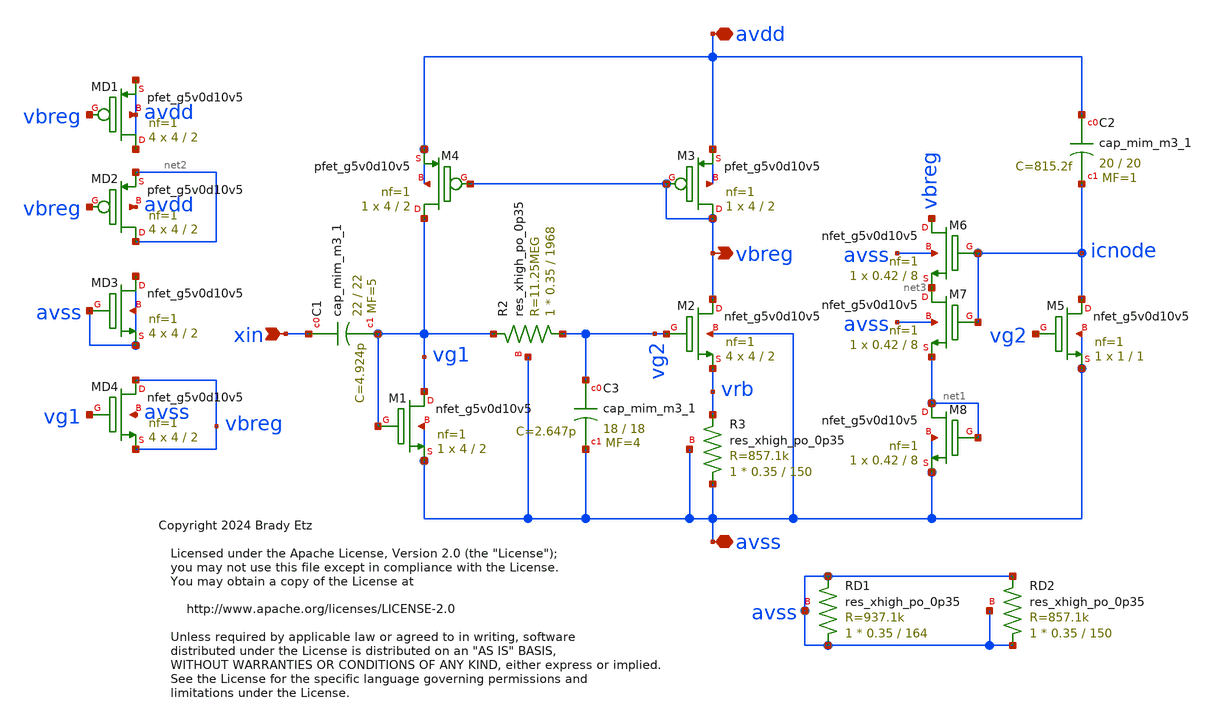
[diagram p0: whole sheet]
** sch_path: xschem/bias_gen.sch
* Copyright 2024 Brady Etz
* Licensed under the Apache License, Version 2.0 (the "License");
**.subckt bias_gen xin avdd avss vbreg
*.ipin xin
*.iopin avdd
*.iopin avss
*.opin vbreg
XM2 vbreg vg2 vrb avss sky130_fd_pr__nfet_g5v0d10v5 L=2 W=4 nf=1 ad='int((nf+1)/2) * W/nf * 0.29' as='int((nf+2)/2) * W/nf * 0.29'
+ pd='2*int((nf+1)/2) * (W/nf + 0.29)' ps='2*int((nf+2)/2) * (W/nf + 0.29)' nrd='0.29 / W' nrs='0.29 / W'
+ sa=0 sb=0 sd=0 mult=4 m=4
XM3 vbreg vbreg avdd avdd sky130_fd_pr__pfet_g5v0d10v5 L=2 W=4 nf=1 ad='int((nf+1)/2) * W/nf * 0.29'
+ as='int((nf+2)/2) * W/nf * 0.29' pd='2*int((nf+1)/2) * (W/nf + 0.29)' ps='2*int((nf+2)/2) * (W/nf + 0.29)'
+ nrd='0.29 / W' nrs='0.29 / W' sa=0 sb=0 sd=0 mult=1 m=1
XM4 vg1 vbreg avdd avdd sky130_fd_pr__pfet_g5v0d10v5 L=2 W=4 nf=1 ad='int((nf+1)/2) * W/nf * 0.29' as='int((nf+2)/2) * W/nf * 0.29'
+ pd='2*int((nf+1)/2) * (W/nf + 0.29)' ps='2*int((nf+2)/2) * (W/nf + 0.29)' nrd='0.29 / W' nrs='0.29 / W'
+ sa=0 sb=0 sd=0 mult=1 m=1
XM1 vg1 vg1 avss avss sky130_fd_pr__nfet_g5v0d10v5 L=2 W=4 nf=1 ad='int((nf+1)/2) * W/nf * 0.29' as='int((nf+2)/2) * W/nf * 0.29'
+ pd='2*int((nf+1)/2) * (W/nf + 0.29)' ps='2*int((nf+2)/2) * (W/nf + 0.29)' nrd='0.29 / W' nrs='0.29 / W'
+ sa=0 sb=0 sd=0 mult=1 m=1
XR2 vg2 vg1 avss sky130_fd_pr__res_xhigh_po_0p35 L=1968 mult=1 m=1
XR3 avss vrb avss sky130_fd_pr__res_xhigh_po_0p35 L=150 mult=1 m=1
XC3 vg2 avss sky130_fd_pr__cap_mim_m3_1 W=18 L=18 MF=4 m=4
XC1 xin vg1 sky130_fd_pr__cap_mim_m3_1 W=22 L=22 MF=5 m=5
XM5 icnode vg2 avss avss sky130_fd_pr__nfet_g5v0d10v5 L=1 W=1 nf=1 ad='int((nf+1)/2) * W/nf * 0.29' as='int((nf+2)/2) * W/nf * 0.29'
+ pd='2*int((nf+1)/2) * (W/nf + 0.29)' ps='2*int((nf+2)/2) * (W/nf + 0.29)' nrd='0.29 / W' nrs='0.29 / W'
+ sa=0 sb=0 sd=0 mult=1 m=1
XC2 avdd icnode sky130_fd_pr__cap_mim_m3_1 W=20 L=20 MF=1 m=1
XM6 vbreg icnode net3 avss sky130_fd_pr__nfet_g5v0d10v5 L=8 W=0.42 nf=1 ad='int((nf+1)/2) * W/nf * 0.29'
+ as='int((nf+2)/2) * W/nf * 0.29' pd='2*int((nf+1)/2) * (W/nf + 0.29)' ps='2*int((nf+2)/2) * (W/nf + 0.29)'
+ nrd='0.29 / W' nrs='0.29 / W' sa=0 sb=0 sd=0 mult=1 m=1
XM8 net1 net1 avss avss sky130_fd_pr__nfet_g5v0d10v5 L=8 W=0.42 nf=1 ad='int((nf+1)/2) * W/nf * 0.29'
+ as='int((nf+2)/2) * W/nf * 0.29' pd='2*int((nf+1)/2) * (W/nf + 0.29)' ps='2*int((nf+2)/2) * (W/nf + 0.29)'
+ nrd='0.29 / W' nrs='0.29 / W' sa=0 sb=0 sd=0 mult=1 m=1
XM7 net3 icnode net1 avss sky130_fd_pr__nfet_g5v0d10v5 L=8 W=0.42 nf=1 ad='int((nf+1)/2) * W/nf * 0.29'
+ as='int((nf+2)/2) * W/nf * 0.29' pd='2*int((nf+1)/2) * (W/nf + 0.29)' ps='2*int((nf+2)/2) * (W/nf + 0.29)'
+ nrd='0.29 / W' nrs='0.29 / W' sa=0 sb=0 sd=0 mult=1 m=1
XRD1 avss avss avss sky130_fd_pr__res_xhigh_po_0p35 L=164 mult=1 m=1
XRD2 avss avss avss sky130_fd_pr__res_xhigh_po_0p35 L=150 mult=1 m=1
XMD1 avdd vbreg avdd avdd sky130_fd_pr__pfet_g5v0d10v5 L=2 W=4 nf=1 ad='int((nf+1)/2) * W/nf * 0.29'
+ as='int((nf+2)/2) * W/nf * 0.29' pd='2*int((nf+1)/2) * (W/nf + 0.29)' ps='2*int((nf+2)/2) * (W/nf + 0.29)'
+ nrd='0.29 / W' nrs='0.29 / W' sa=0 sb=0 sd=0 mult=4 m=4
XMD2 net2 vbreg net2 avdd sky130_fd_pr__pfet_g5v0d10v5 L=2 W=4 nf=1 ad='int((nf+1)/2) * W/nf * 0.29'
+ as='int((nf+2)/2) * W/nf * 0.29' pd='2*int((nf+1)/2) * (W/nf + 0.29)' ps='2*int((nf+2)/2) * (W/nf + 0.29)'
+ nrd='0.29 / W' nrs='0.29 / W' sa=0 sb=0 sd=0 mult=4 m=4
XMD3 avss avss avss avss sky130_fd_pr__nfet_g5v0d10v5 L=2 W=4 nf=1 ad='int((nf+1)/2) * W/nf * 0.29' as='int((nf+2)/2) * W/nf * 0.29'
+ pd='2*int((nf+1)/2) * (W/nf + 0.29)' ps='2*int((nf+2)/2) * (W/nf + 0.29)' nrd='0.29 / W' nrs='0.29 / W'
+ sa=0 sb=0 sd=0 mult=4 m=4
XMD4 vbreg vg1 vbreg avss sky130_fd_pr__nfet_g5v0d10v5 L=2 W=4 nf=1 ad='int((nf+1)/2) * W/nf * 0.29'
+ as='int((nf+2)/2) * W/nf * 0.29' pd='2*int((nf+1)/2) * (W/nf + 0.29)' ps='2*int((nf+2)/2) * (W/nf + 0.29)'
+ nrd='0.29 / W' nrs='0.29 / W' sa=0 sb=0 sd=0 mult=4 m=4
**.ends
.end
